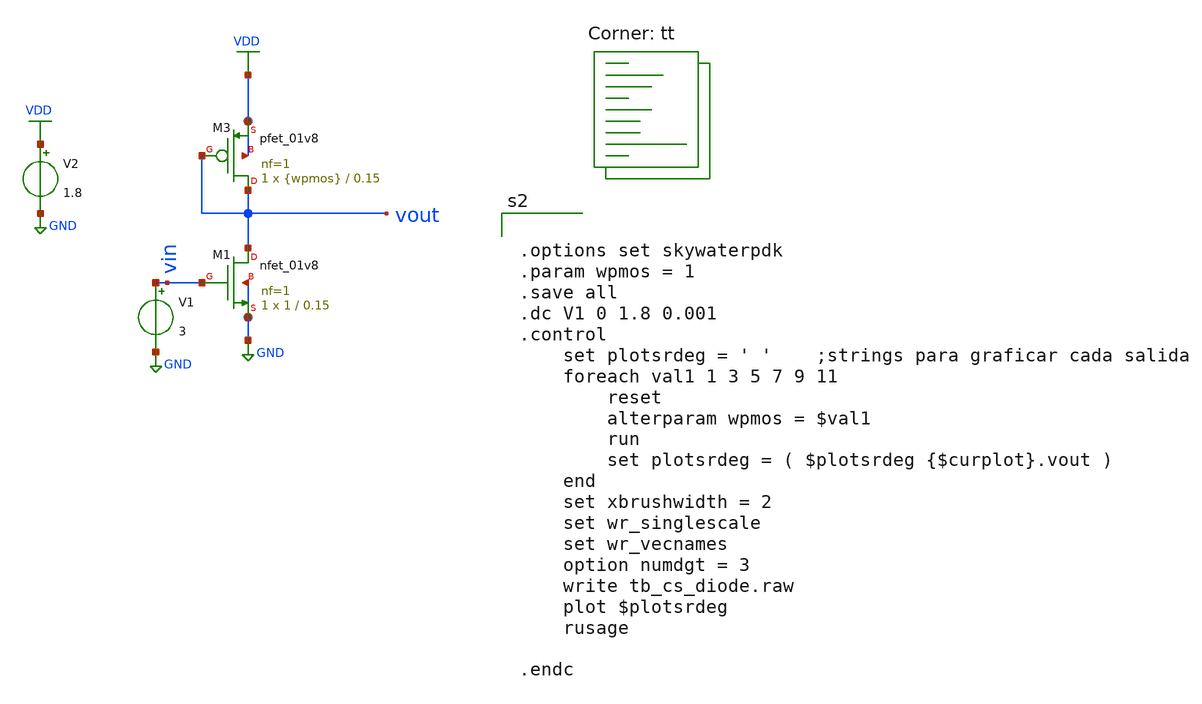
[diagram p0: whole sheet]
** sch_path: cs_diode.sch
**.subckt cs_diode
XM1 vout vin GND GND sky130_fd_pr__nfet_01v8 L=0.15 W=1 nf=1 ad='int((1 + 1)/2) * 1 / 1 * 0.29' as='int((1 + 2)/2) * 1 / 1 * 0.29'
+ pd='2*int((1 + 1)/2) * (1 / 1 + 0.29)' ps='2*int((1 + 2)/2) * (1 / 1 + 0.29)' nrd='0.29 / 1 ' nrs='0.29 / 1 '
+ sa=0 sb=0 sd=0 mult=1 m=1
XM3 vout vout VDD VDD sky130_fd_pr__pfet_01v8 L=0.15 W={wpmos} nf=1 ad='int((1 + 1)/2) * {wpmos} / 1 * 0.29'
+ as='int((1 + 2)/2) * {wpmos} / 1 * 0.29' pd='2*int((1 + 1)/2) * ({wpmos} / 1 + 0.29)' ps='2*int((1 + 2)/2) * ({wpmos} / 1 + 0.29)'
+ nrd='0.29 / {wpmos} ' nrs='0.29 / {wpmos} ' sa=0 sb=0 sd=0 mult=1 m=1
V1 vin GND 3
V2 VDD GND 1.8
**** begin user architecture code
.lib $::SKYWATER_MODELS/sky130.lib.spice tt


.options set skywaterpdk
.param wpmos = 1
.save all
.dc V1 0 1.8 0.001
.control
	set plotsrdeg = ' '	;strings para graficar cada salida
	foreach val1 1 3 5 7 9 11
		reset
		alterparam wpmos = $val1
		run
		set plotsrdeg = ( $plotsrdeg {$curplot}.vout )
	end
	set xbrushwidth = 2
	set wr_singlescale
	set wr_vecnames
	option numdgt = 3
	write tb_cs_diode.raw
	plot $plotsrdeg
	rusage

.endc


**** end user architecture code
**.ends
.GLOBAL GND
.GLOBAL VDD
.end
